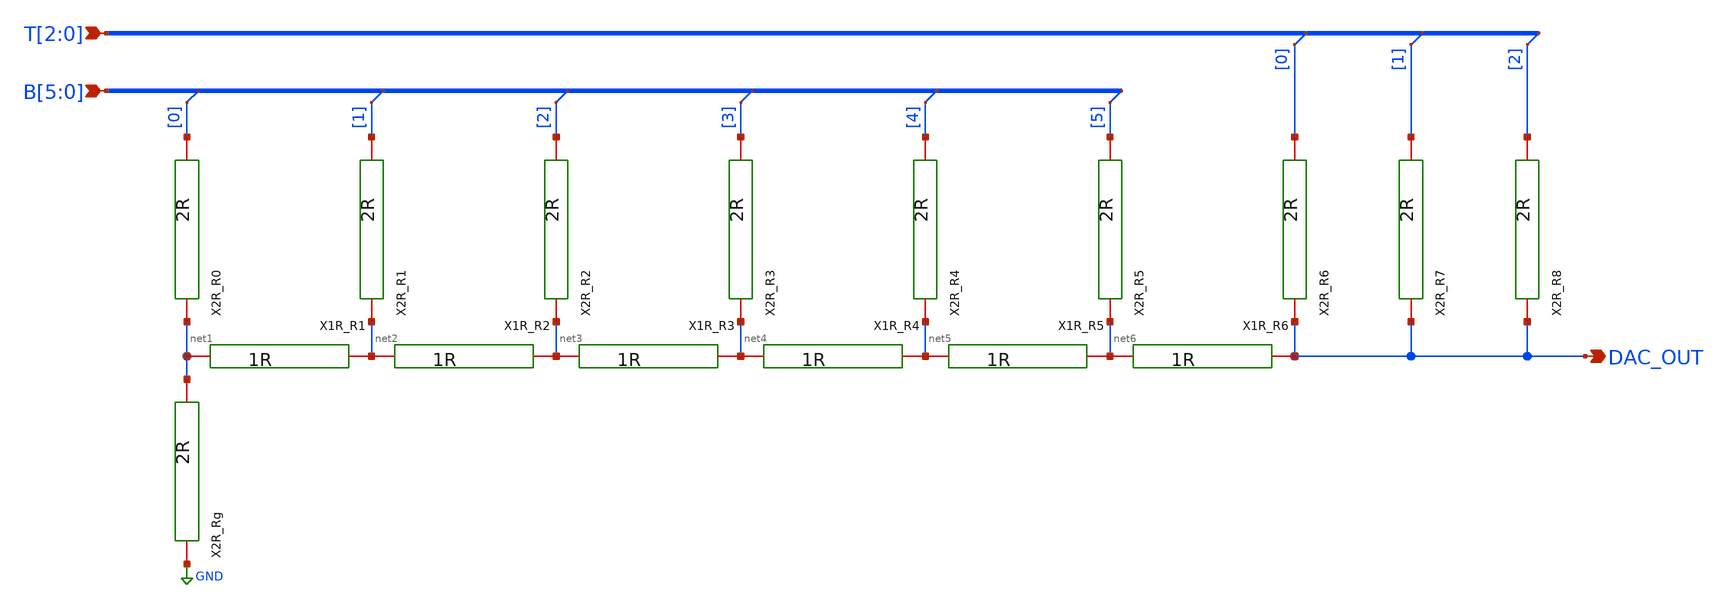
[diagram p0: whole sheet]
** sch_path: xschem/dac.sch
**.subckt dac B[5],B[4],B[3],B[2],B[1],B[0] T[2],T[1],T[0] DAC_OUT
*.ipin B[5],B[4],B[3],B[2],B[1],B[0]
*.ipin T[2],T[1],T[0]
*.opin DAC_OUT
X1R_R1 net1 net2 1R
X2R_R0 B[0] net1 2R
X2R_Rg net1 GND 2R
X2R_R1 B[1] net2 2R
X1R_R2 net2 net3 1R
X2R_R2 B[2] net3 2R
X1R_R3 net3 net4 1R
X2R_R3 B[3] net4 2R
X1R_R4 net4 net5 1R
X2R_R4 B[4] net5 2R
X1R_R5 net5 net6 1R
X2R_R5 B[5] net6 2R
X1R_R6 net6 DAC_OUT 1R
X2R_R6 T[0] DAC_OUT 2R
X2R_R7 T[1] DAC_OUT 2R
X2R_R8 T[2] DAC_OUT 2R
* tap: B[5:0] --> B[0]
* tap: B[5:0] --> B[1]
* tap: B[5:0] --> B[2]
* tap: B[5:0] --> B[3]
* tap: B[5:0] --> B[4]
* tap: B[5:0] --> B[5]
* tap: T[2:0] --> T[0]
* tap: T[2:0] --> T[1]
* tap: T[2:0] --> T[2]
**.ends

* expanding   symbol:  /home/j542yu/Documents/ece298a-msk-modem/xschem/1R.sym # of pins=2
** sym_path: xschem/1R.sym
** sch_path: xschem/1R.sch
.subckt 1R 1R_1 1R_2
*.iopin 1R_1
*.iopin 1R_2
XR1 net1 1R_1 GND ppolyf_u_1k r_width=2e-6 r_length=30e-6 m=1
XR29 1R_2 net1 GND ppolyf_u_1k r_width=2e-6 r_length=30e-6 m=1
.ends


* expanding   symbol:  /home/j542yu/Documents/ece298a-msk-modem/xschem/2R.sym # of pins=2
** sym_path: xschem/2R.sym
** sch_path: xschem/2R.sch
.subckt 2R 2R_1 2R_2
*.iopin 2R_1
*.iopin 2R_2
XR1 net1 2R_1 GND ppolyf_u_1k r_width=2e-6 r_length=30e-6 m=1
XR29 net2 net1 GND ppolyf_u_1k r_width=2e-6 r_length=30e-6 m=1
XR2 net3 net2 GND ppolyf_u_1k r_width=2e-6 r_length=30e-6 m=1
XR3 2R_2 net3 GND ppolyf_u_1k r_width=2e-6 r_length=30e-6 m=1
.ends

.GLOBAL GND
.end
